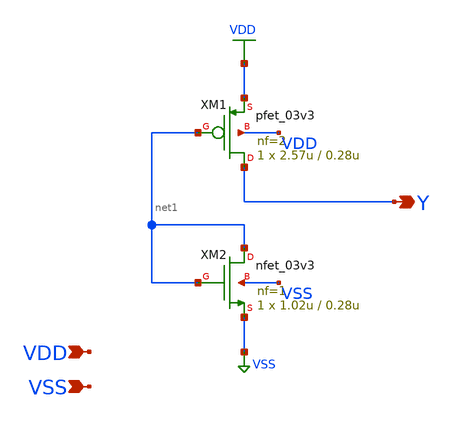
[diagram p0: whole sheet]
** sch_path: xschem/gf180mcu_ocd_sc_rt12t3v3__tieh.sch
**.subckt gf180mcu_ocd_sc_rt12t3v3__tieh Y VDD VSS
*.opin Y
*.ipin VDD
*.ipin VSS
XM1 Y net1 VDD VDD pfet_03v3 L=0.28u W=2.57u nf=2 ad='int((nf+1)/2) * W/nf * 0.18u' as='int((nf+2)/2) * W/nf * 0.18u'
+ pd='2*int((nf+1)/2) * (W/nf + 0.18u)' ps='2*int((nf+2)/2) * (W/nf + 0.18u)' nrd='0.18u / W' nrs='0.18u / W'
+ sa=0 sb=0 sd=0 m=1
XM2 net1 net1 VSS VSS nfet_03v3 L=0.28u W=1.02u nf=1 ad='int((nf+1)/2) * W/nf * 0.18u' as='int((nf+2)/2) * W/nf * 0.18u'
+ pd='2*int((nf+1)/2) * (W/nf + 0.18u)' ps='2*int((nf+2)/2) * (W/nf + 0.18u)' nrd='0.18u / W' nrs='0.18u / W'
+ sa=0 sb=0 sd=0 m=1
**.ends
.GLOBAL VDD
.GLOBAL VSS
.end
